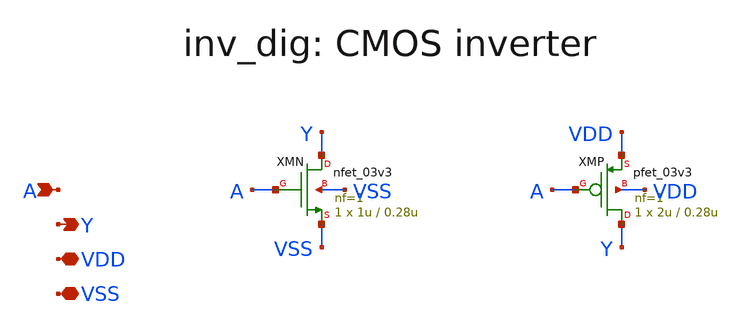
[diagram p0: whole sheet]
** sch_path: v1_claude/xschem/inv_dig.sch
**.subckt inv_dig A Y VDD VSS
*.ipin A
*.opin Y
*.iopin VDD
*.iopin VSS
XMN Y A VSS VSS nfet_03v3 L=0.28u W=1u nf=1 ad='int((nf+1)/2) * W/nf * 0.18u' as='int((nf+2)/2) * W/nf * 0.18u'
+ pd='2*int((nf+1)/2) * (W/nf + 0.18u)' ps='2*int((nf+2)/2) * (W/nf + 0.18u)' nrd='0.18u / W' nrs='0.18u / W'
+ sa=0 sb=0 sd=0 m=1
XMP Y A VDD VDD pfet_03v3 L=0.28u W=2u nf=1 ad='int((nf+1)/2) * W/nf * 0.18u' as='int((nf+2)/2) * W/nf * 0.18u'
+ pd='2*int((nf+1)/2) * (W/nf + 0.18u)' ps='2*int((nf+2)/2) * (W/nf + 0.18u)' nrd='0.18u / W' nrs='0.18u / W'
+ sa=0 sb=0 sd=0 m=1
**.ends
.end
